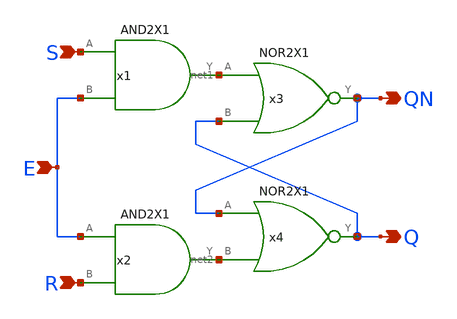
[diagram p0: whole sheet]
** sch_path: lib/xschem/SRELATCH.sch
**.subckt SRELATCH S R QN Q E
*.ipin S
*.ipin R
*.opin QN
*.opin Q
*.ipin E
x1 net1 S E VDD VSS AND2X1
x2 net2 E R VDD VSS AND2X1
x3 QN net1 Q VDD VSS NOR2X1
x4 Q QN net2 VDD VSS NOR2X1
**.ends
.end
